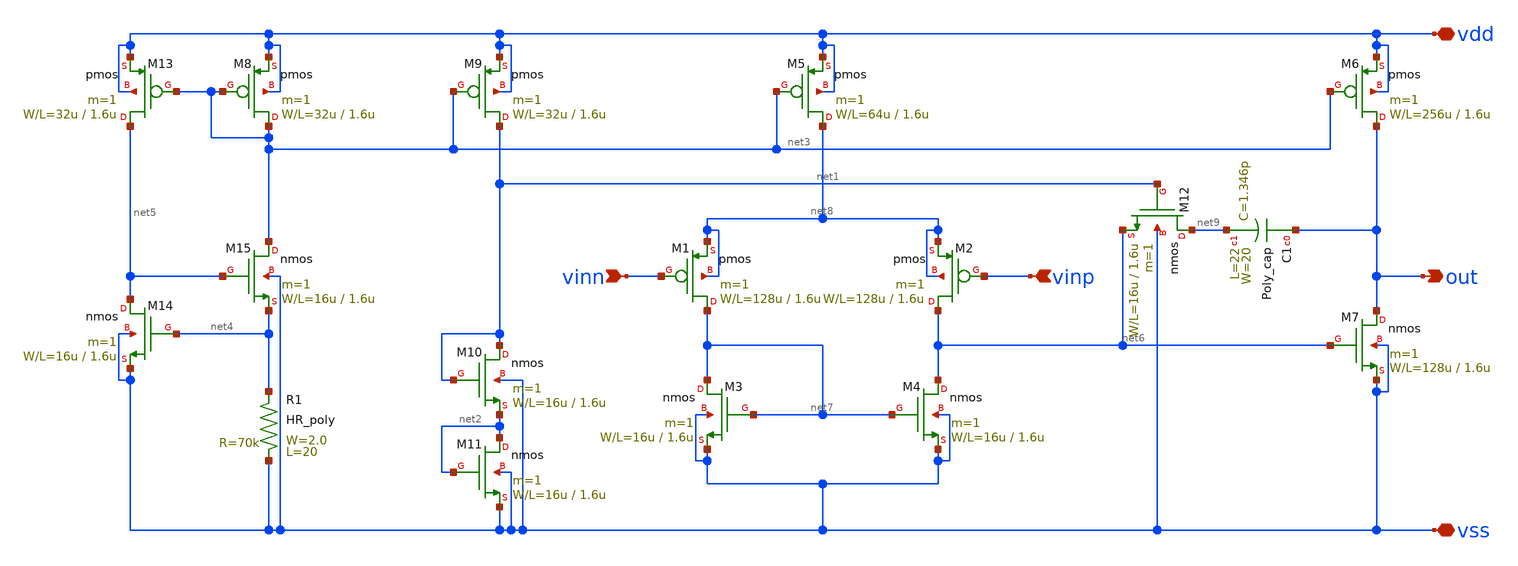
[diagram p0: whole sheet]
** sch_path: member_project/GroupWork/Team_Ando/dokunira/sch/opamp_cs_full.sch
**.subckt opamp_cs_full vdd vss vinn vinp out
*.iopin vdd
*.iopin vss
*.ipin vinn
*.ipin vinp
*.opin out
M12 net9 net1 net6 vss nmos L=1.6u W=16u m=1
M9 net1 net3 vdd vdd pmos L=1.6u W=32u m=1
M10 net1 net1 net2 vss nmos L=1.6u W=16u m=1
M11 net2 net2 vss vss nmos L=1.6u W=16u m=1
R1 vss net4 HR_poly W=2.0 L=20
M8 net3 net3 vdd vdd pmos L=1.6u W=32u m=1
M13 net5 net3 vdd vdd pmos L=1.6u W=32u m=1
M15 net3 net5 net4 vss nmos L=1.6u W=16u m=1
M14 net5 net4 vss vss nmos L=1.6u W=16u m=1
M5 net8 net3 vdd vdd pmos L=1.6u W=64u m=1
M1 net7 vinn net8 net8 pmos L=1.6u W=128u m=1
M2 net6 vinp net8 net8 pmos L=1.6u W=128u m=1
M3 net7 net7 vss vss nmos L=1.6u W=16u m=1
M4 net6 net7 vss vss nmos L=1.6u W=16u m=1
M6 out net3 vdd vdd pmos L=1.6u W=256u m=1
M7 out net6 vss vss nmos L=1.6u W=128u m=1
C1 out net9 Poly_cap W=20 L=22
**.ends
.end
